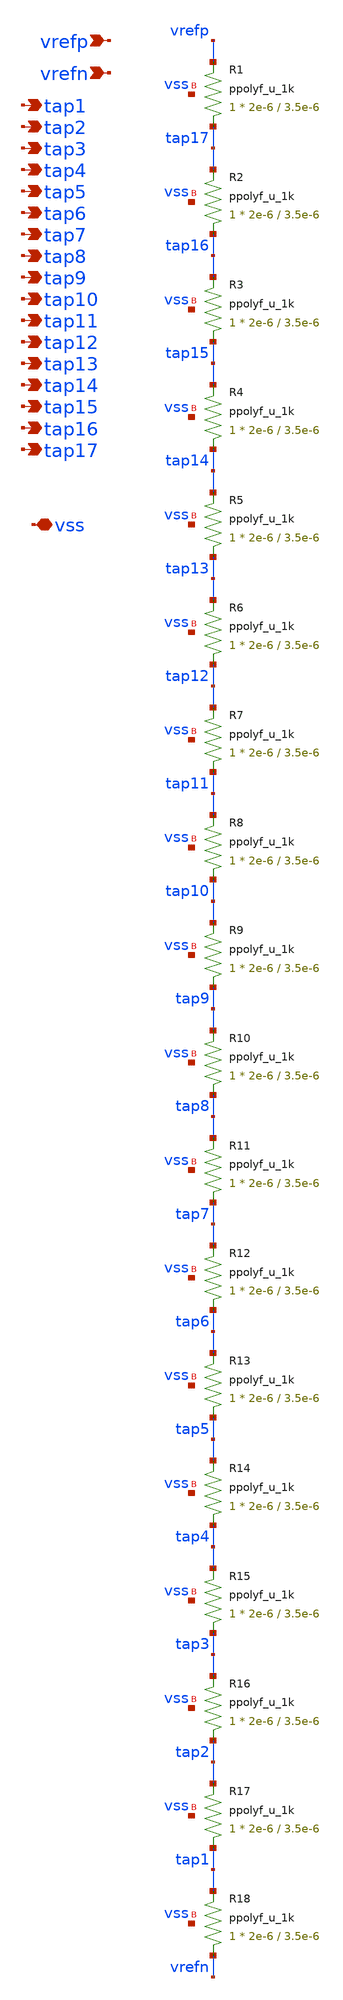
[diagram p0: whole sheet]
** sch_path: blocks/adc/comp-array/ladder.sch
**.subckt ladder vrefp vrefn tap1 tap2 tap3 tap4 tap5 tap6 tap7 tap8 tap9 tap10 tap11 tap12 tap13
*+ tap14 tap15 tap16 tap17 vss
*.ipin vrefp
*.ipin vrefn
*.opin tap1
*.opin tap2
*.opin tap3
*.opin tap4
*.opin tap5
*.opin tap6
*.opin tap7
*.opin tap8
*.opin tap9
*.opin tap10
*.opin tap11
*.opin tap12
*.opin tap13
*.opin tap14
*.opin tap15
*.opin tap16
*.opin tap17
*.iopin vss
XR1 tap17 vrefp vss ppolyf_u_1k r_width=2e-6 r_length=3.5e-6 m=1
XR2 tap16 tap17 vss ppolyf_u_1k r_width=2e-6 r_length=3.5e-6 m=1
XR3 tap15 tap16 vss ppolyf_u_1k r_width=2e-6 r_length=3.5e-6 m=1
XR4 tap14 tap15 vss ppolyf_u_1k r_width=2e-6 r_length=3.5e-6 m=1
XR5 tap13 tap14 vss ppolyf_u_1k r_width=2e-6 r_length=3.5e-6 m=1
XR6 tap12 tap13 vss ppolyf_u_1k r_width=2e-6 r_length=3.5e-6 m=1
XR7 tap11 tap12 vss ppolyf_u_1k r_width=2e-6 r_length=3.5e-6 m=1
XR8 tap10 tap11 vss ppolyf_u_1k r_width=2e-6 r_length=3.5e-6 m=1
XR9 tap9 tap10 vss ppolyf_u_1k r_width=2e-6 r_length=3.5e-6 m=1
XR10 tap8 tap9 vss ppolyf_u_1k r_width=2e-6 r_length=3.5e-6 m=1
XR11 tap7 tap8 vss ppolyf_u_1k r_width=2e-6 r_length=3.5e-6 m=1
XR12 tap6 tap7 vss ppolyf_u_1k r_width=2e-6 r_length=3.5e-6 m=1
XR13 tap5 tap6 vss ppolyf_u_1k r_width=2e-6 r_length=3.5e-6 m=1
XR14 tap4 tap5 vss ppolyf_u_1k r_width=2e-6 r_length=3.5e-6 m=1
XR15 tap3 tap4 vss ppolyf_u_1k r_width=2e-6 r_length=3.5e-6 m=1
XR16 tap2 tap3 vss ppolyf_u_1k r_width=2e-6 r_length=3.5e-6 m=1
XR17 tap1 tap2 vss ppolyf_u_1k r_width=2e-6 r_length=3.5e-6 m=1
XR18 vrefn tap1 vss ppolyf_u_1k r_width=2e-6 r_length=3.5e-6 m=1
**.ends
.end
